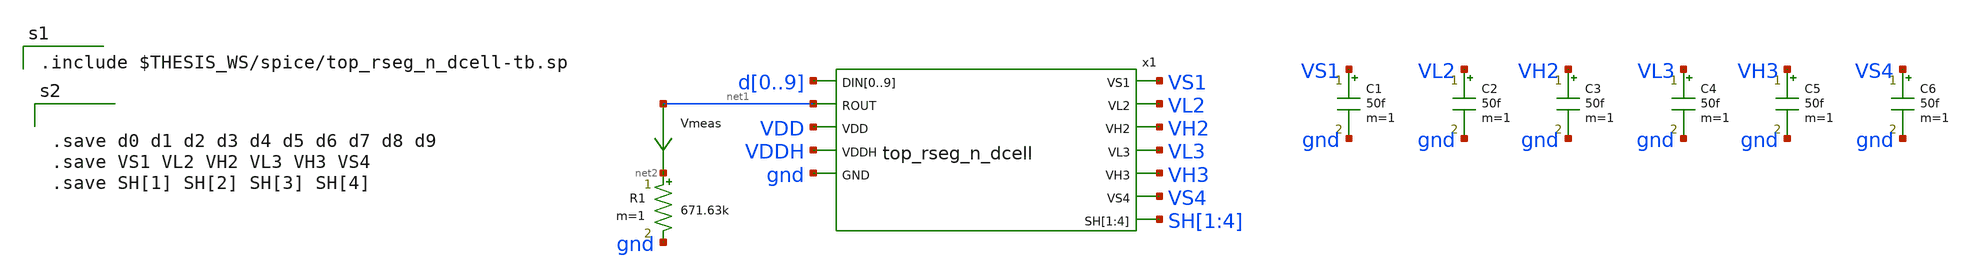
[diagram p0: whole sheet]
** sch_path: xschem/top_rseg_n_dcell-tb.sch
.lib $::SKYWATER_MODELS/sky130.lib.spice tt
.include $::SKYWATER_STDCELLS/sky130_fd_sc_hd.spice
.include ~/pdk/sky130A/libs.ref/sky130_fd_sc_hvl/spice/sky130_fd_sc_hvl.spice

**.subckt top_rseg_n_dcell-tb
R1 net2 gnd 671.63k m=1
C1 VS1 gnd 50f m=1
C2 VL2 gnd 50f m=1
C3 VH2 gnd 50f m=1
C4 VL3 gnd 50f m=1
C5 VH3 gnd 50f m=1
C6 VS4 gnd 50f m=1
Vmeas net1 net2 0
.save i(vmeas)
x1 d0 d1 d2 d3 d4 d5 d6 d7 d8 d9 net1 VS1 VL2 VH2 VL3 VH3 VS4 SH[1] SH[2] SH[3] SH[4] VDD VDDH gnd
+ top_rseg_n_dcell
**** begin user architecture code

.include $THESIS_WS/spice/top_rseg_n_dcell-tb.sp



.save d0 d1 d2 d3 d4 d5 d6 d7 d8 d9
.save VS1 VL2 VH2 VL3 VH3 VS4
.save SH[1] SH[2] SH[3] SH[4]


**** end user architecture code
**.ends
.end
